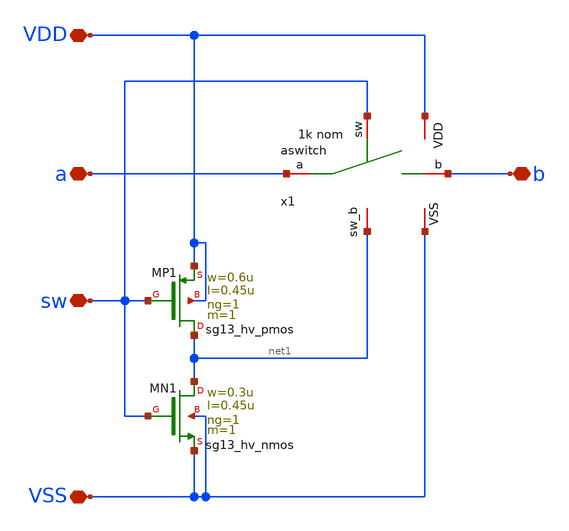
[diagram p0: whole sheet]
** sch_path: macros/heichips26_FAIf/macros/asw_inv/schematic/xschem/asw_inv.sch
**.subckt asw_inv a sw VDD b VSS
*.iopin a
*.iopin sw
*.iopin VDD
*.iopin b
*.iopin VSS
x1 net1 VDD b a VSS sw aswitch
XMP1 net1 sw VDD VDD sg13_hv_pmos w=0.6u l=0.45u ng=1 m=1 mm_ok=1
XMN1 net1 sw VSS VSS sg13_hv_nmos w=0.3u l=0.45u ng=1 m=1 mm_ok=1
**.ends
.end
